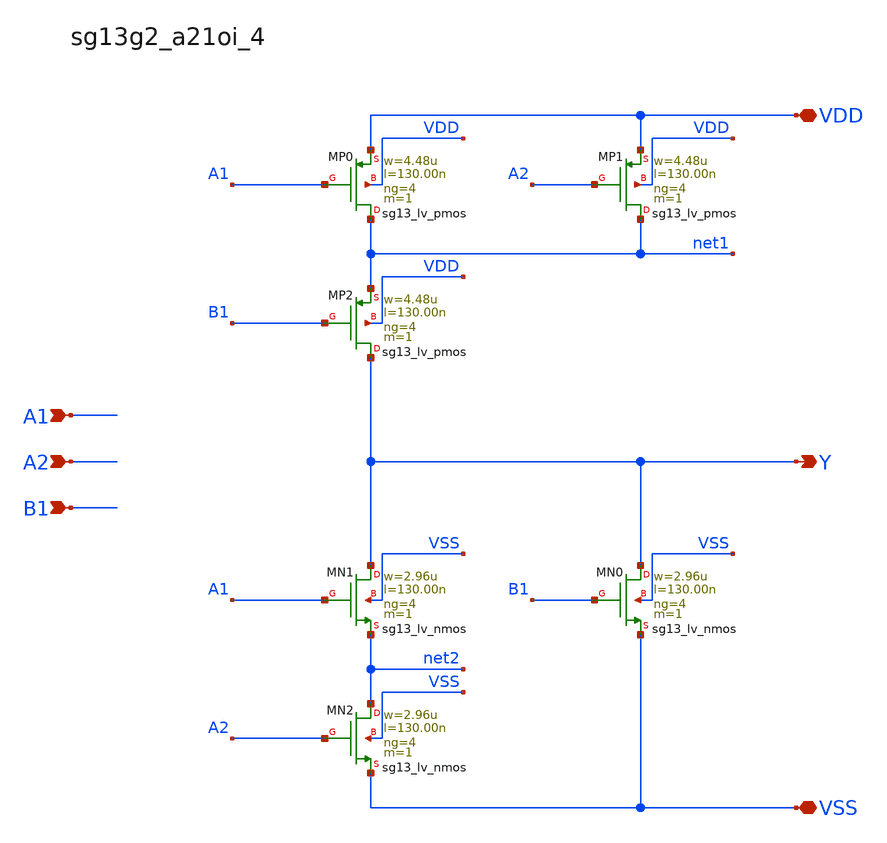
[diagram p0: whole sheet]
** sch_path: outputs/sg13g2_cells/cells/sg13g2_a21oi_4/sg13g2_a21oi_4.sch
**.subckt sg13g2_a21oi_4 Y A1 A2 B1 VDD VSS
*.opin Y
*.ipin A1
*.ipin A2
*.ipin B1
*.iopin VDD
*.iopin VSS
XMN0 Y B1 VSS VSS sg13_lv_nmos w=2.96u l=130.00n ng=4 m=1 mm_ok=1
XMN2 net2 A2 VSS VSS sg13_lv_nmos w=2.96u l=130.00n ng=4 m=1 mm_ok=1
XMN1 Y A1 net2 VSS sg13_lv_nmos w=2.96u l=130.00n ng=4 m=1 mm_ok=1
XMP2 Y B1 net1 VDD sg13_lv_pmos w=4.48u l=130.00n ng=4 m=1 mm_ok=1
XMP1 net1 A2 VDD VDD sg13_lv_pmos w=4.48u l=130.00n ng=4 m=1 mm_ok=1
XMP0 net1 A1 VDD VDD sg13_lv_pmos w=4.48u l=130.00n ng=4 m=1 mm_ok=1
**.ends
.end
